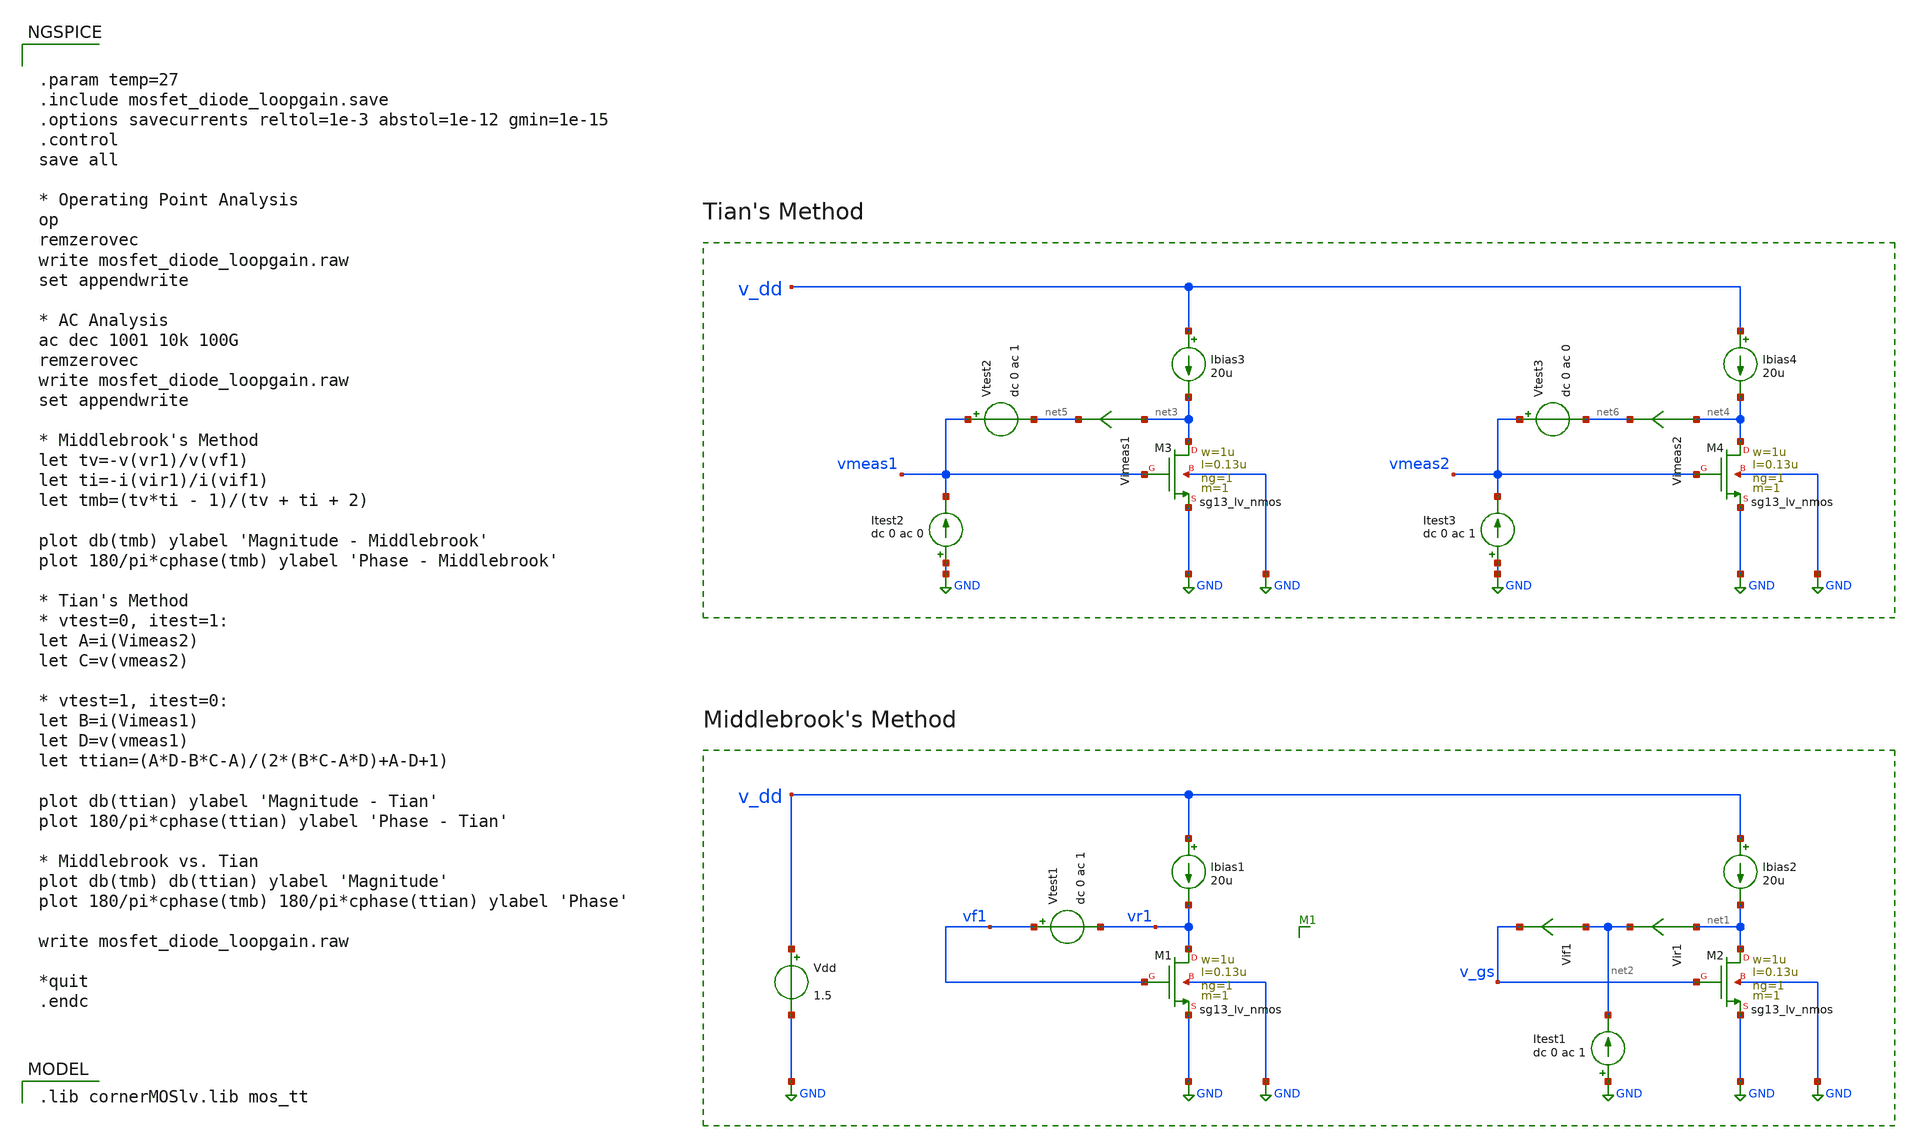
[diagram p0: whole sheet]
** sch_path: xschem/mosfet_diode_loopgain.sch
* (c) 2024-2025 H. Pretl, S. Dorrer, Apache-2.0 license
**.subckt mosfet_diode_loopgain
Vdd v_dd GND 1.5
XM1 vr1 vf1 GND GND sg13_lv_nmos w=1u l=0.13u ng=1 m=1 mm_ok=1
Ibias1 v_dd vr1 20u
Vtest1 vf1 vr1 dc 0 ac 1
XM2 net1 v_gs GND GND sg13_lv_nmos w=1u l=0.13u ng=1 m=1 mm_ok=1
Ibias2 v_dd net1 20u
Vir1 net1 net2 0
.save i(vir1)
Vif1 net2 v_gs 0
.save i(vif1)
Itest1 GND net2 dc 0 ac 1
XM3 net3 vmeas1 GND GND sg13_lv_nmos w=1u l=0.13u ng=1 m=1 mm_ok=1
Ibias3 v_dd net3 20u
XM4 net4 vmeas2 GND GND sg13_lv_nmos w=1u l=0.13u ng=1 m=1 mm_ok=1
Ibias4 v_dd net4 20u
Itest2 GND vmeas1 dc 0 ac 0
Itest3 GND vmeas2 dc 0 ac 1
Vtest2 vmeas1 net5 dc 0 ac 1
Vtest3 vmeas2 net6 dc 0 ac 0
Vimeas1 net3 net5 0
.save i(vimeas1)
Vimeas2 net4 net6 0
.save i(vimeas2)
**** begin user architecture code
 .lib cornerMOSlv.lib mos_tt



.param temp=27
.include mosfet_diode_loopgain.save
.options savecurrents reltol=1e-3 abstol=1e-12 gmin=1e-15
.control
save all

* Operating Point Analysis
op
remzerovec
write mosfet_diode_loopgain.raw
set appendwrite

* AC Analysis
ac dec 1001 10k 100G
remzerovec
write mosfet_diode_loopgain.raw
set appendwrite

* Middlebrook's Method
let tv=-v(vr1)/v(vf1)
let ti=-i(vir1)/i(vif1)
let tmb=(tv*ti - 1)/(tv + ti + 2)

plot db(tmb) ylabel 'Magnitude - Middlebrook'
plot 180/pi*cphase(tmb) ylabel 'Phase - Middlebrook'

* Tian's Method
* vtest=0, itest=1:
let A=i(Vimeas2)
let C=v(vmeas2)

* vtest=1, itest=0:
let B=i(Vimeas1)
let D=v(vmeas1)
let ttian=(A*D-B*C-A)/(2*(B*C-A*D)+A-D+1)

plot db(ttian) ylabel 'Magnitude - Tian'
plot 180/pi*cphase(ttian) ylabel 'Phase - Tian'

* Middlebrook vs. Tian
plot db(tmb) db(ttian) ylabel 'Magnitude'
plot 180/pi*cphase(tmb) 180/pi*cphase(ttian) ylabel 'Phase'

write mosfet_diode_loopgain.raw

*quit
.endc


**** end user architecture code
**.ends
.GLOBAL GND
.end
